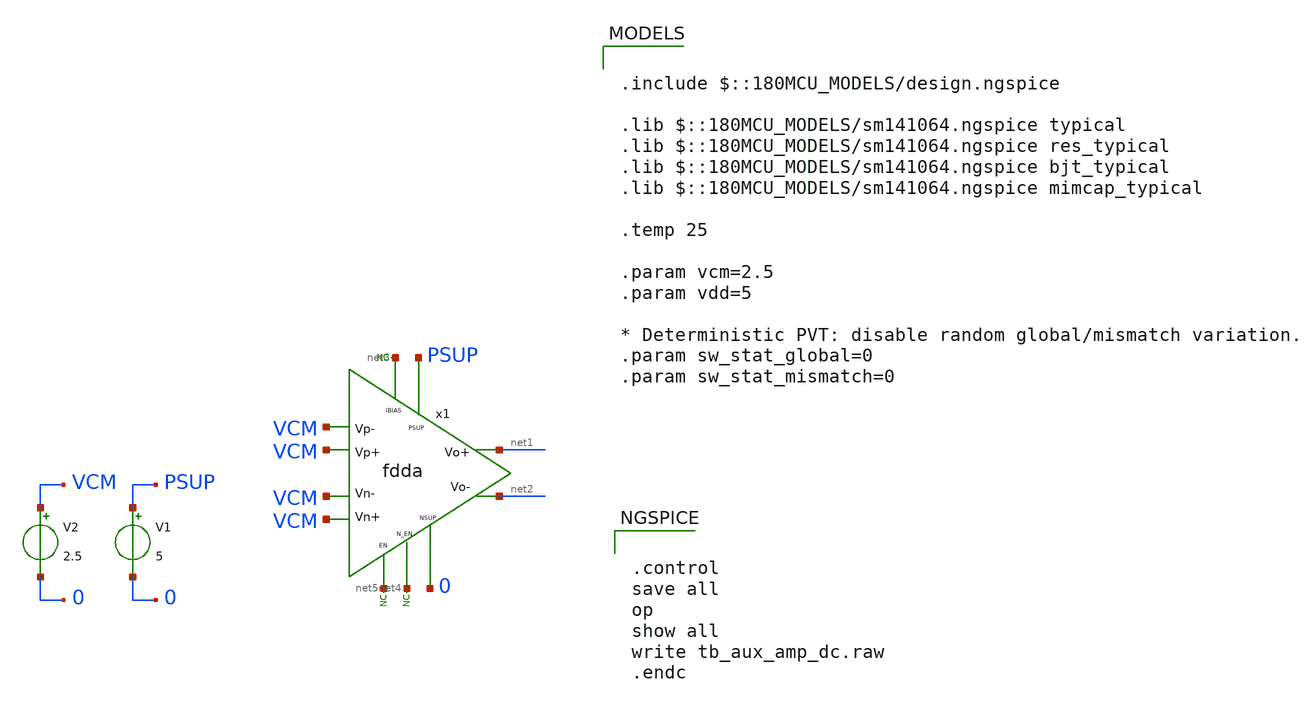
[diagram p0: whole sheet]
** sch_path: xschem/blocks/fdda/tb_fdda_dc.sch
**.subckt tb_fdda_dc
x1 PSUP VCM VCM VCM VCM net1 net2 net3 net4 net5 0 fdda
* noconn #net3
* noconn #net5
* noconn #net4
V1 PSUP 0 5
V2 VCM 0 2.5
**** begin user architecture code


.control
save all
op
show all
write tb_aux_amp_dc.raw
.endc



.include $::180MCU_MODELS/design.ngspice

.lib $::180MCU_MODELS/sm141064.ngspice typical
.lib $::180MCU_MODELS/sm141064.ngspice res_typical
.lib $::180MCU_MODELS/sm141064.ngspice bjt_typical
.lib $::180MCU_MODELS/sm141064.ngspice mimcap_typical

.temp 25

.param vcm=2.5
.param vdd=5

* Deterministic PVT: disable random global/mismatch variation.
.param sw_stat_global=0
.param sw_stat_mismatch=0


**** end user architecture code
**.ends

* expanding   symbol:  blocks/fdda/fdda.sym # of pins=11
** sym_path: xschem/blocks/fdda/fdda.sym
** sch_path: xschem/blocks/fdda/fdda.sch
.subckt fdda PSUP Vp- Vn+ Vn- Vp+ Vo+ Vo- IBIAS N_EN EN NSUP
*.ipin PSUP
*.ipin NSUP
*.ipin N_EN
*.ipin EN
*.ipin IBIAS
*.ipin Vp+
*.ipin Vp-
*.ipin Vn+
*.ipin Vn-
*.opin Vo+
*.opin Vo-
* noconn N_EN
* noconn EN
I0 net5 NSUP 1u
XM9 Vo+ Vp- net1 NSUP pfet_06v0 L=2u W=4u nf=5 ad='int((nf+1)/2) * W/nf * 0.18u' as='int((nf+2)/2) * W/nf * 0.18u'
+ pd='2*int((nf+1)/2) * (W/nf + 0.18u)' ps='2*int((nf+2)/2) * (W/nf + 0.18u)' nrd='0.18u / W' nrs='0.18u / W'
+ sa=0 sb=0 sd=0 m=10
XM1 Vo- Vp+ net1 NSUP pfet_06v0 L=2u W=4u nf=5 ad='int((nf+1)/2) * W/nf * 0.18u' as='int((nf+2)/2) * W/nf * 0.18u'
+ pd='2*int((nf+1)/2) * (W/nf + 0.18u)' ps='2*int((nf+2)/2) * (W/nf + 0.18u)' nrd='0.18u / W' nrs='0.18u / W'
+ sa=0 sb=0 sd=0 m=10
XM2 net1 vb1 PSUP net3 pfet_06v0 L=4u W=2u nf=1 ad='int((nf+1)/2) * W/nf * 0.18u' as='int((nf+2)/2) * W/nf * 0.18u'
+ pd='2*int((nf+1)/2) * (W/nf + 0.18u)' ps='2*int((nf+2)/2) * (W/nf + 0.18u)' nrd='0.18u / W' nrs='0.18u / W'
+ sa=0 sb=0 sd=0 m=8
XM3 Vo- Vo- NSUP NSUP nfet_06v0 L=4u W=2u nf=1 ad='int((nf+1)/2) * W/nf * 0.18u' as='int((nf+2)/2) * W/nf * 0.18u'
+ pd='2*int((nf+1)/2) * (W/nf + 0.18u)' ps='2*int((nf+2)/2) * (W/nf + 0.18u)' nrd='0.18u / W' nrs='0.18u / W'
+ sa=0 sb=0 sd=0 m=4
XM4 Vo+ Vn- net2 NSUP pfet_06v0 L=2u W=4u nf=5 ad='int((nf+1)/2) * W/nf * 0.18u' as='int((nf+2)/2) * W/nf * 0.18u'
+ pd='2*int((nf+1)/2) * (W/nf + 0.18u)' ps='2*int((nf+2)/2) * (W/nf + 0.18u)' nrd='0.18u / W' nrs='0.18u / W'
+ sa=0 sb=0 sd=0 m=10
XM5 Vo- Vn+ net2 NSUP pfet_06v0 L=2u W=4u nf=5 ad='int((nf+1)/2) * W/nf * 0.18u' as='int((nf+2)/2) * W/nf * 0.18u'
+ pd='2*int((nf+1)/2) * (W/nf + 0.18u)' ps='2*int((nf+2)/2) * (W/nf + 0.18u)' nrd='0.18u / W' nrs='0.18u / W'
+ sa=0 sb=0 sd=0 m=10
XM6 net2 vb1 PSUP PSUP pfet_06v0 L=4u W=2u nf=1 ad='int((nf+1)/2) * W/nf * 0.18u' as='int((nf+2)/2) * W/nf * 0.18u'
+ pd='2*int((nf+1)/2) * (W/nf + 0.18u)' ps='2*int((nf+2)/2) * (W/nf + 0.18u)' nrd='0.18u / W' nrs='0.18u / W'
+ sa=0 sb=0 sd=0 m=8
XM8 Vo+ Vo+ NSUP NSUP nfet_06v0 L=4u W=2u nf=1 ad='int((nf+1)/2) * W/nf * 0.18u' as='int((nf+2)/2) * W/nf * 0.18u'
+ pd='2*int((nf+1)/2) * (W/nf + 0.18u)' ps='2*int((nf+2)/2) * (W/nf + 0.18u)' nrd='0.18u / W' nrs='0.18u / W'
+ sa=0 sb=0 sd=0 m=4
XM7 net5 vb1 PSUP net4 pfet_06v0 L=4u W=2u nf=1 ad='int((nf+1)/2) * W/nf * 0.18u' as='int((nf+2)/2) * W/nf * 0.18u'
+ pd='2*int((nf+1)/2) * (W/nf + 0.18u)' ps='2*int((nf+2)/2) * (W/nf + 0.18u)' nrd='0.18u / W' nrs='0.18u / W'
+ sa=0 sb=0 sd=0 m=4
.ends

.end
